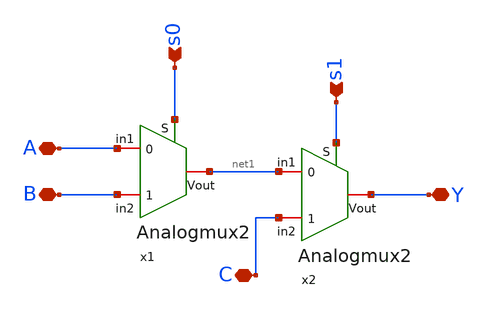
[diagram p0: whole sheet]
** sch_path: xschem/Final/mux3analog.sch
**.subckt mux3analog A B C Y s0 s1
*.iopin A
*.iopin B
*.iopin C
*.iopin Y
*.ipin s0
*.ipin s1
x1 s0 A net1 B Analogmux2
x2 s1 net1 Y C Analogmux2
**.ends
.end
